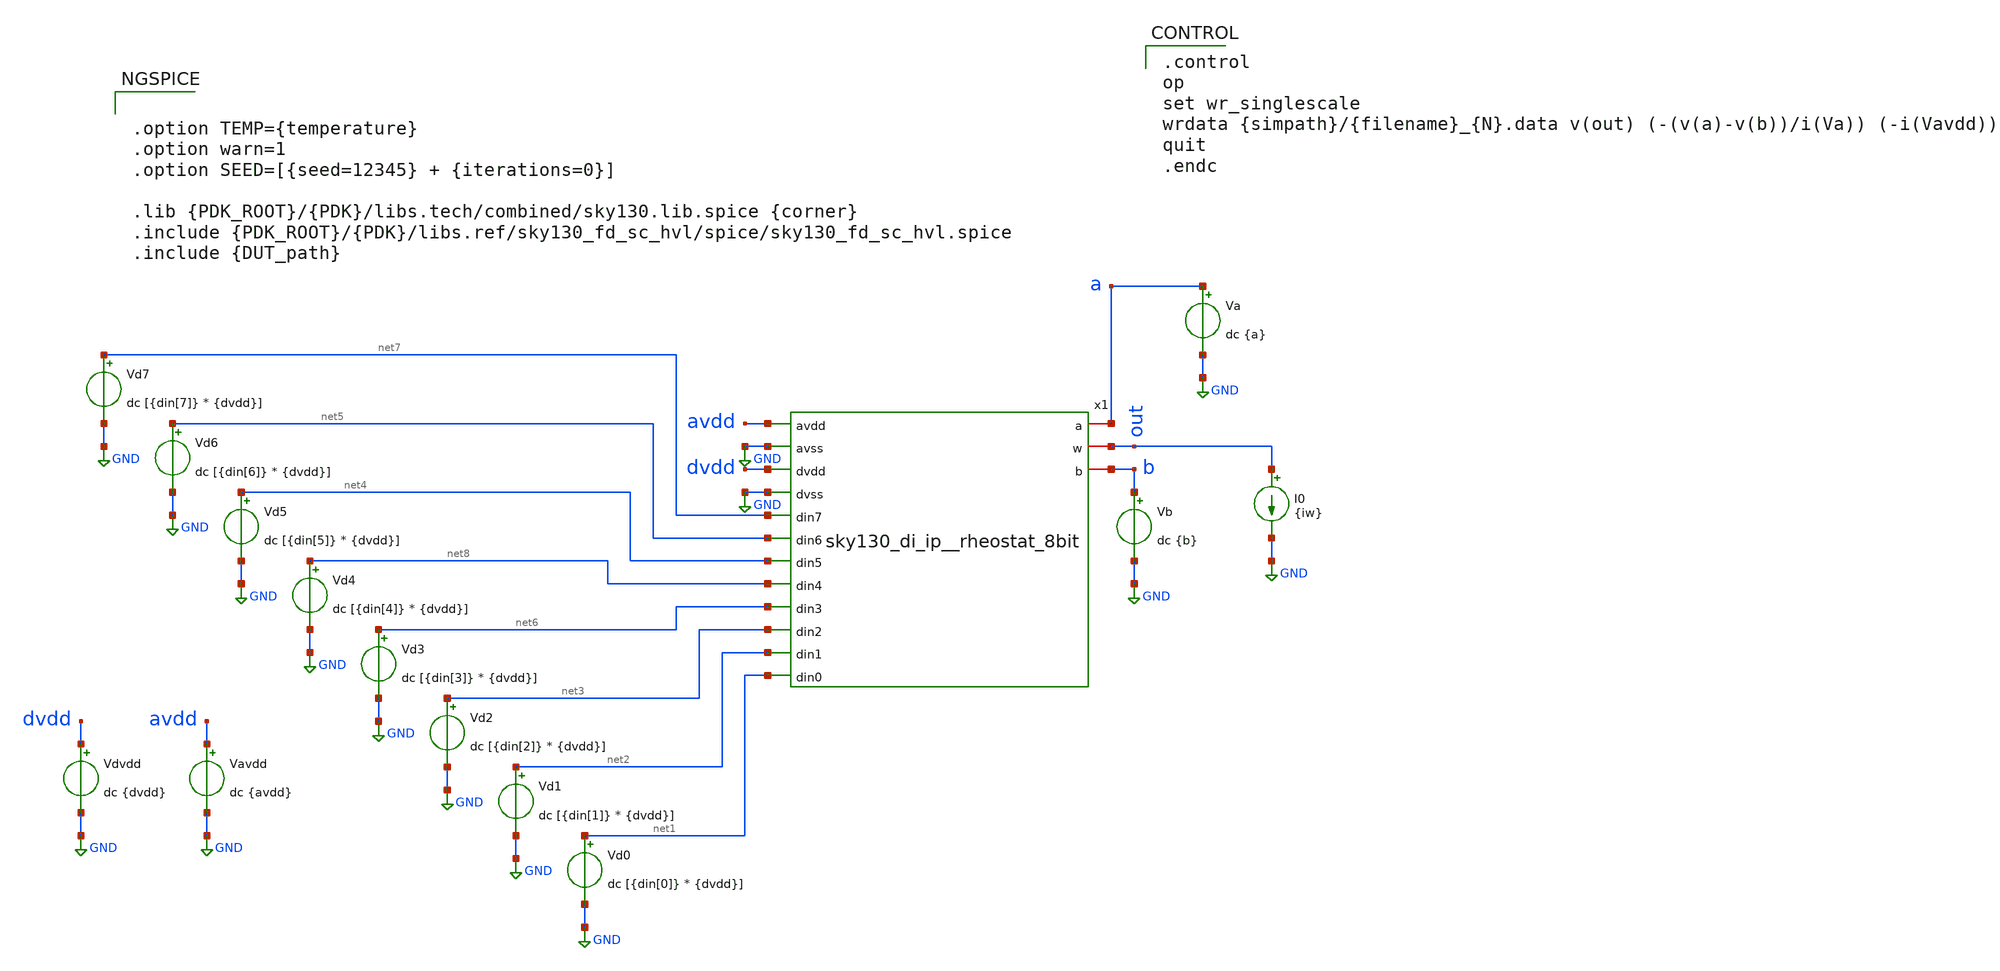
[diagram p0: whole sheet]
** sch_path: cace/tb_op_mc.sch
**.subckt tb_op_mc
x1 avdd GND dvdd GND net7 net5 net4 a net8 net6 out net3 net2 net1 b sky130_di_ip__rheostat_8bit
Vd0 net1 GND dc [{din[0]} * {dvdd}]
Vd1 net2 GND dc [{din[1]} * {dvdd}]
Vd2 net3 GND dc [{din[2]} * {dvdd}]
Vd3 net6 GND dc [{din[3]} * {dvdd}]
Vd4 net8 GND dc [{din[4]} * {dvdd}]
Vd5 net4 GND dc [{din[5]} * {dvdd}]
Vd6 net5 GND dc [{din[6]} * {dvdd}]
Vd7 net7 GND dc [{din[7]} * {dvdd}]
Vdvdd dvdd GND dc {dvdd}
Vavdd avdd GND dc {avdd}
Va a GND dc {a}
Vb b GND dc {b}
I0 out GND {iw}
**** begin user architecture code


.option TEMP={temperature}
.option warn=1
.option SEED=[{seed=12345} + {iterations=0}]

.lib {PDK_ROOT}/{PDK}/libs.tech/combined/sky130.lib.spice {corner}
.include {PDK_ROOT}/{PDK}/libs.ref/sky130_fd_sc_hvl/spice/sky130_fd_sc_hvl.spice
.include {DUT_path}



.control
op
set wr_singlescale
wrdata {simpath}/{filename}_{N}.data v(out) (-(v(a)-v(b))/i(Va)) (-i(Vavdd))
quit
.endc


**** end user architecture code
**.ends
.GLOBAL GND
.end
